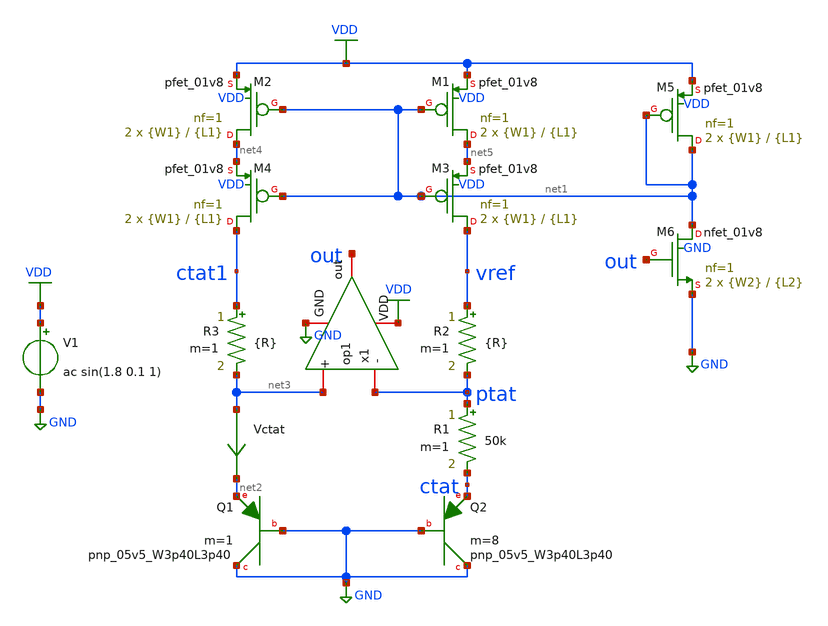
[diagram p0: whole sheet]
** sch_path: xschem/bgr_op1.sch
**.subckt bgr_op1
XQ1 GND GND net2 sky130_fd_pr__pnp_05v5_W3p40L3p40 m=1
XQ2 GND GND ctat sky130_fd_pr__pnp_05v5_W3p40L3p40 m=8
R1 ptat ctat 50k m=1
Vctat net3 net2 0
.save i(vctat)
V1 VDD GND ac sin(1.8 0.1 1)
x1 VDD out ptat net3 GND op1
XM1 net5 net1 VDD VDD sky130_fd_pr__pfet_01v8 L={L1} W={W1} nf=1 ad='int((nf+1)/2) * W/nf * 0.29' as='int((nf+2)/2) * W/nf * 0.29'
+ pd='2*int((nf+1)/2) * (W/nf + 0.29)' ps='2*int((nf+2)/2) * (W/nf + 0.29)' nrd='0.29 / W' nrs='0.29 / W'
+ sa=0 sb=0 sd=0 mult=2 m=2
XM2 net4 net1 VDD VDD sky130_fd_pr__pfet_01v8 L={L1} W={W1} nf=1 ad='int((nf+1)/2) * W/nf * 0.29' as='int((nf+2)/2) * W/nf * 0.29'
+ pd='2*int((nf+1)/2) * (W/nf + 0.29)' ps='2*int((nf+2)/2) * (W/nf + 0.29)' nrd='0.29 / W' nrs='0.29 / W'
+ sa=0 sb=0 sd=0 mult=2 m=2
R2 vref ptat {R} m=1
R3 ctat1 net3 {R} m=1
XM3 vref net1 net5 VDD sky130_fd_pr__pfet_01v8 L={L1} W={W1} nf=1 ad='int((nf+1)/2) * W/nf * 0.29' as='int((nf+2)/2) * W/nf * 0.29'
+ pd='2*int((nf+1)/2) * (W/nf + 0.29)' ps='2*int((nf+2)/2) * (W/nf + 0.29)' nrd='0.29 / W' nrs='0.29 / W'
+ sa=0 sb=0 sd=0 mult=2 m=2
XM4 ctat1 net1 net4 VDD sky130_fd_pr__pfet_01v8 L={L1} W={W1} nf=1 ad='int((nf+1)/2) * W/nf * 0.29' as='int((nf+2)/2) * W/nf * 0.29'
+ pd='2*int((nf+1)/2) * (W/nf + 0.29)' ps='2*int((nf+2)/2) * (W/nf + 0.29)' nrd='0.29 / W' nrs='0.29 / W'
+ sa=0 sb=0 sd=0 mult=2 m=2
XM5 net1 net1 VDD VDD sky130_fd_pr__pfet_01v8 L={L1} W={W1} nf=1 ad='int((nf+1)/2) * W/nf * 0.29' as='int((nf+2)/2) * W/nf * 0.29'
+ pd='2*int((nf+1)/2) * (W/nf + 0.29)' ps='2*int((nf+2)/2) * (W/nf + 0.29)' nrd='0.29 / W' nrs='0.29 / W'
+ sa=0 sb=0 sd=0 mult=2 m=2
XM6 net1 out GND GND sky130_fd_pr__nfet_01v8 L={L2} W={W2} nf=1 ad='int((nf+1)/2) * W/nf * 0.29' as='int((nf+2)/2) * W/nf * 0.29'
+ pd='2*int((nf+1)/2) * (W/nf + 0.29)' ps='2*int((nf+2)/2) * (W/nf + 0.29)' nrd='0.29 / W' nrs='0.29 / W'
+ sa=0 sb=0 sd=0 mult=2 m=2
**** begin user architecture code


.param L1=5
.param W1=1
.param R=489k
.param L2=20
.param W2=1



** opencircuitdesign pdks install
.lib $::SKYWATER_MODELS/sky130.lib.spice tt




.option savecurrents
.control
save all
op
remzerovec
write bgr_op1.raw
set appendwrite

dc temp -40 85 1
remzerovec
write bgr_op1.raw
plot (ptat-ctat)
plot ctat
plot vref

********TC********
meas dc temp_avg_vref avg v(vref)
meas dc temp_vref_27 find v(vref) when temp-sweep=27
meas dc temp_pp_vref PP v(vref)
meas dc temp_vref_max max v(vref)
meas dc temp_max_vref when v(vref)='temp_vref_max'
meas dc temp_vref_min min v(vref)
meas dc temp_min_vref when v(vref)='temp_vref_min'
let vref_tc='((temp_pp_vref*1000000)/(125*temp_avg_vref))'
print vref_tc

******PSRR******
ac dec 1000 1 10Meg
write bgr_op1.raw
remzerovec
plot vdb(vref)
meas ac psrr find vdb(vref) at=1k

****Power****
tran 0.1 0.5
write bgr_op1.raw
remzerovec
meas tran ave_v avg vdd
meas tran ave_i avg i(v1)
let ave_power='ave_v*(-ave_i)
plot vdd vref
*plot i(vvref)
print ave_power

*******LS******
dc v1 0 3.5 0.1
write bgr_op1.raw
remzerovec
meas dc vref_max max v(vref) from=1.62 to=1.98
meas dc vref_min min v(vref) from=1.62 to=1.98
let ls='(vref_max-vref_min)/(1.98-1.62)'
print ls

.endc


**** end user architecture code
**.ends

* expanding   symbol:  op1.sym # of pins=5
** sym_path: xschem/op1.sym
** sch_path: xschem/op1.sch
.subckt op1 VDD out - + GND
*.iopin VDD
*.iopin GND
*.iopin -
*.iopin +
*.iopin out
**** begin user architecture code


.param L=20
.param W=1


**** end user architecture code
C2 out net5 2.2p m=1
R2 net5 net1 850k m=1
XM1 bias bias GND GND sky130_fd_pr__nfet_01v8 L={L} W={W/1.5} nf=1 ad='int((nf+1)/2) * W/nf * 0.29' as='int((nf+2)/2)
+ * W/nf * 0.29' pd='2*int((nf+1)/2) * (W/nf + 0.29)' ps='2*int((nf+2)/2) * (W/nf + 0.29)' nrd='0.29 /
+ W' nrs='0.29 / W' sa=0 sb=0 sd=0 mult=2 m=2
XM2 net4 bias GND GND sky130_fd_pr__nfet_01v8 L={L} W={W/1.5} nf=1 ad='int((nf+1)/2) * W/nf * 0.29' as='int((nf+2)/2)
+ * W/nf * 0.29' pd='2*int((nf+1)/2) * (W/nf + 0.29)' ps='2*int((nf+2)/2) * (W/nf + 0.29)' nrd='0.29 /
+ W' nrs='0.29 / W' sa=0 sb=0 sd=0 mult=2 m=2
XM3 net2 - net3 GND sky130_fd_pr__nfet_01v8 L={L} W={W} nf=1 ad='int((nf+1)/2) * W/nf * 0.29' as='int((nf+2)/2)
+ * W/nf * 0.29' pd='2*int((nf+1)/2) * (W/nf + 0.29)' ps='2*int((nf+2)/2) * (W/nf + 0.29)' nrd='0.29 /
+ W' nrs='0.29 / W' sa=0 sb=0 sd=0 mult=4 m=4
XM4 net1 + net3 GND sky130_fd_pr__nfet_01v8 L={L} W={W} nf=1 ad='int((nf+1)/2) * W/nf * 0.29' as='int((nf+2)/2)
+ * W/nf * 0.29' pd='2*int((nf+1)/2) * (W/nf + 0.29)' ps='2*int((nf+2)/2) * (W/nf + 0.29)' nrd='0.29 /
+ W' nrs='0.29 / W' sa=0 sb=0 sd=0 mult=4 m=4
XM6 bias net4 VDD VDD sky130_fd_pr__pfet_01v8 L={L} W={W/1.5} nf=1 ad='int((nf+1)/2) * W/nf * 0.29' as='int((nf+2)/2)
+ * W/nf * 0.29' pd='2*int((nf+1)/2) * (W/nf + 0.29)' ps='2*int((nf+2)/2) * (W/nf + 0.29)' nrd='0.29 /
+ W' nrs='0.29 / W' sa=0 sb=0 sd=0 mult=2 m=2
XM7 net4 net4 VDD VDD sky130_fd_pr__pfet_01v8 L={L} W={W/1.5} nf=1 ad='int((nf+1)/2) * W/nf * 0.29' as='int((nf+2)/2)
+ * W/nf * 0.29' pd='2*int((nf+1)/2) * (W/nf + 0.29)' ps='2*int((nf+2)/2) * (W/nf + 0.29)' nrd='0.29 /
+ W' nrs='0.29 / W' sa=0 sb=0 sd=0 mult=2 m=2
XM8 net1 net2 VDD VDD sky130_fd_pr__pfet_01v8 L={L} W={W} nf=1 ad='int((nf+1)/2) * W/nf * 0.29' as='int((nf+2)/2)
+ * W/nf * 0.29' pd='2*int((nf+1)/2) * (W/nf + 0.29)' ps='2*int((nf+2)/2) * (W/nf + 0.29)' nrd='0.29 /
+ W' nrs='0.29 / W' sa=0 sb=0 sd=0 mult=4 m=4
XM9 net2 net2 VDD VDD sky130_fd_pr__pfet_01v8 L={L} W={W} nf=1 ad='int((nf+1)/2) * W/nf * 0.29' as='int((nf+2)/2)
+ * W/nf * 0.29' pd='2*int((nf+1)/2) * (W/nf + 0.29)' ps='2*int((nf+2)/2) * (W/nf + 0.29)' nrd='0.29 /
+ W' nrs='0.29 / W' sa=0 sb=0 sd=0 mult=4 m=4
XM5 net3 bias GND GND sky130_fd_pr__nfet_01v8 L={L} W={W} nf=1 ad='int((nf+1)/2) * W/nf * 0.29' as='int((nf+2)/2)
+ * W/nf * 0.29' pd='2*int((nf+1)/2) * (W/nf + 0.29)' ps='2*int((nf+2)/2) * (W/nf + 0.29)' nrd='0.29 /
+ W' nrs='0.29 / W' sa=0 sb=0 sd=0 mult=4 m=4
XM10 out net1 VDD VDD sky130_fd_pr__pfet_01v8 L={L} W={W*1.1} nf=1 ad='int((nf+1)/2) * W/nf * 0.29' as='int((nf+2)/2)
+ * W/nf * 0.29' pd='2*int((nf+1)/2) * (W/nf + 0.29)' ps='2*int((nf+2)/2) * (W/nf + 0.29)' nrd='0.29 /
+ W' nrs='0.29 / W' sa=0 sb=0 sd=0 mult=4 m=4
XM11 out bias GND GND sky130_fd_pr__nfet_01v8 L={L} W={W} nf=1 ad='int((nf+1)/2) * W/nf * 0.29' as='int((nf+2)/2)
+ * W/nf * 0.29' pd='2*int((nf+1)/2) * (W/nf + 0.29)' ps='2*int((nf+2)/2) * (W/nf + 0.29)' nrd='0.29 /
+ W' nrs='0.29 / W' sa=0 sb=0 sd=0 mult=2 m=2
.ends

.GLOBAL VDD
.GLOBAL GND
.end
